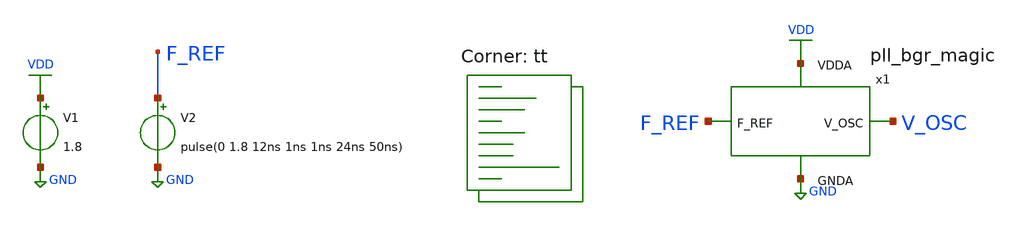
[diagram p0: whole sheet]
** sch_path: projects/pll/full_pll/magic/tb_pll_bgr_magic.sch
**.subckt tb_pll_bgr_magic
V1 VDD GND 1.8
V2 F_REF GND pulse(0 1.8 12ns 1ns 1ns 24ns 50ns)
x1 V_OSC VDD GND F_REF pll_bgr_magic
**** begin user architecture code
.lib $::SKYWATER_MODELS/sky130.lib.spice tt



.include /foss/designs/my_design/projects/pll/full_pll/magic/pll_bgr_magic.spice

.option method=gear
* .option method=trap
.option wnflag=1
* .option savecurrents

.save v(x1.v_cont.n0) v(x1.f_vco.t0) v(x1.pfd_8_0.qa.n0) v(x1.pfd_8_0.qb.n0) v(x1.pfd_8_0.up_input.n0) v(x1.pfd_8_0.down_input.n0) v(x1.charge_pump_cell_6_0.x.n0) v(x1.vco_fd_magic_0.div120_2_0.div2.n0) v(x1.vco_fd_magic_0.div120_2_0.div4.n0) v(x1.vco_fd_magic_0.div120_2_0.div8.n0) v(x1.vco_fd_magic_0.div120_2_0.div24.n0) @m.x1.x58.msky130_fd_pr__pfet_01v8[id] @m.x1.x124.msky130_fd_pr__pfet_01v8[id] @m.x1.x160.msky130_fd_pr__pfet_01v8[id] @m.x1.x161.msky130_fd_pr__pfet_01v8[id] @m.x1.x214.msky130_fd_pr__pfet_01v8[id] @m.x1.x255.msky130_fd_pr__pfet_01v8[id] @m.x1.x382.msky130_fd_pr__pfet_01v8[id] @m.x1.x424.msky130_fd_pr__pfet_01v8[id] @m.x1.x430.msky130_fd_pr__pfet_01v8[id] @m.x1.x463.msky130_fd_pr__pfet_01v8[id]

* V_out initial voltage

.ic v(x1.v_cont.n0) = 0.0


.control
  save v(v_osc)

  * timestep for exact simulation results
  tran 100ps 2us

  remzerovec
  * write tb_pll_bgr_magic.raw
  write tb_pll_bgr_magic_2.raw
  wrdata /foss/designs/my_design/projects/pll/full_pll/magic/tb_pll_bgr_magic_v_osc.txt v(v_osc)
  set appendwrite

.endc



**** end user architecture code
**.ends
.GLOBAL GND
.GLOBAL VDD
.end
